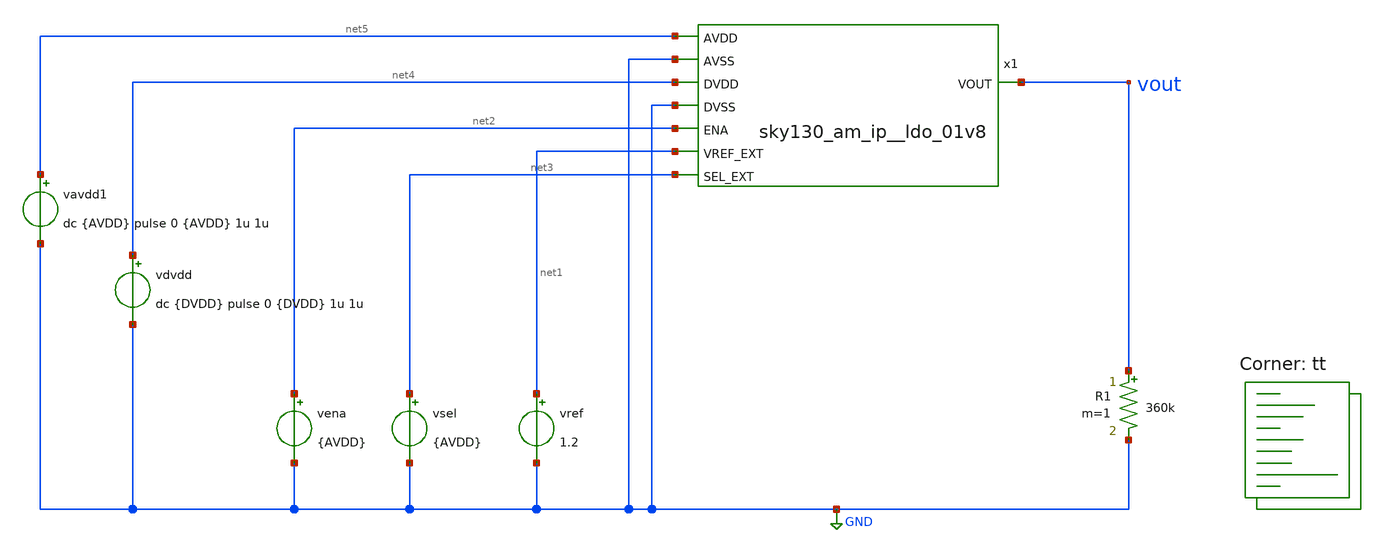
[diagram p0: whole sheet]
** sch_path: xschem/sky130_am_ip__ldo_01v8_tb.sch
**.subckt sky130_am_ip__ldo_01v8_tb
x1 net5 vout GND net2 net1 net3 net4 GND sky130_am_ip__ldo_01v8
R1 vout GND 360k m=1
vdvdd net4 GND dc {DVDD} pulse 0 {DVDD} 1u 1u
vena net2 GND {AVDD}
vref net1 GND 1.2
vsel net3 GND {AVDD}
vavdd1 net5 GND dc {AVDD} pulse 0 {AVDD} 1u 1u
**** begin user architecture code

.option savecurrents
.param AVDD = 3.0
.control
save all

tran 100n 100u
meas tran vout_op find vout at=100u
.endc


.lib $::SKYWATER_MODELS/sky130.lib.spice tt
**** end user architecture code
**.ends
.GLOBAL GND
.end
